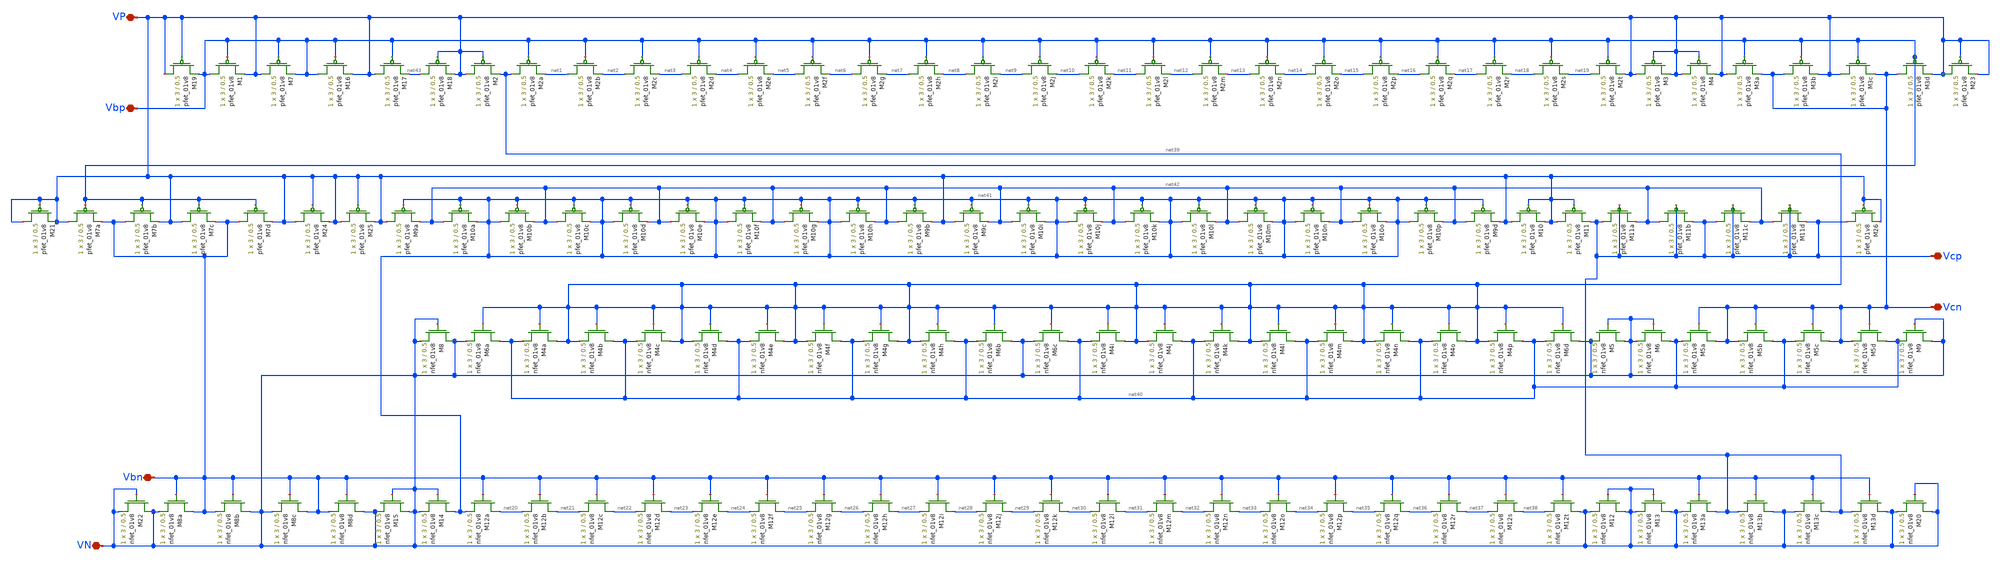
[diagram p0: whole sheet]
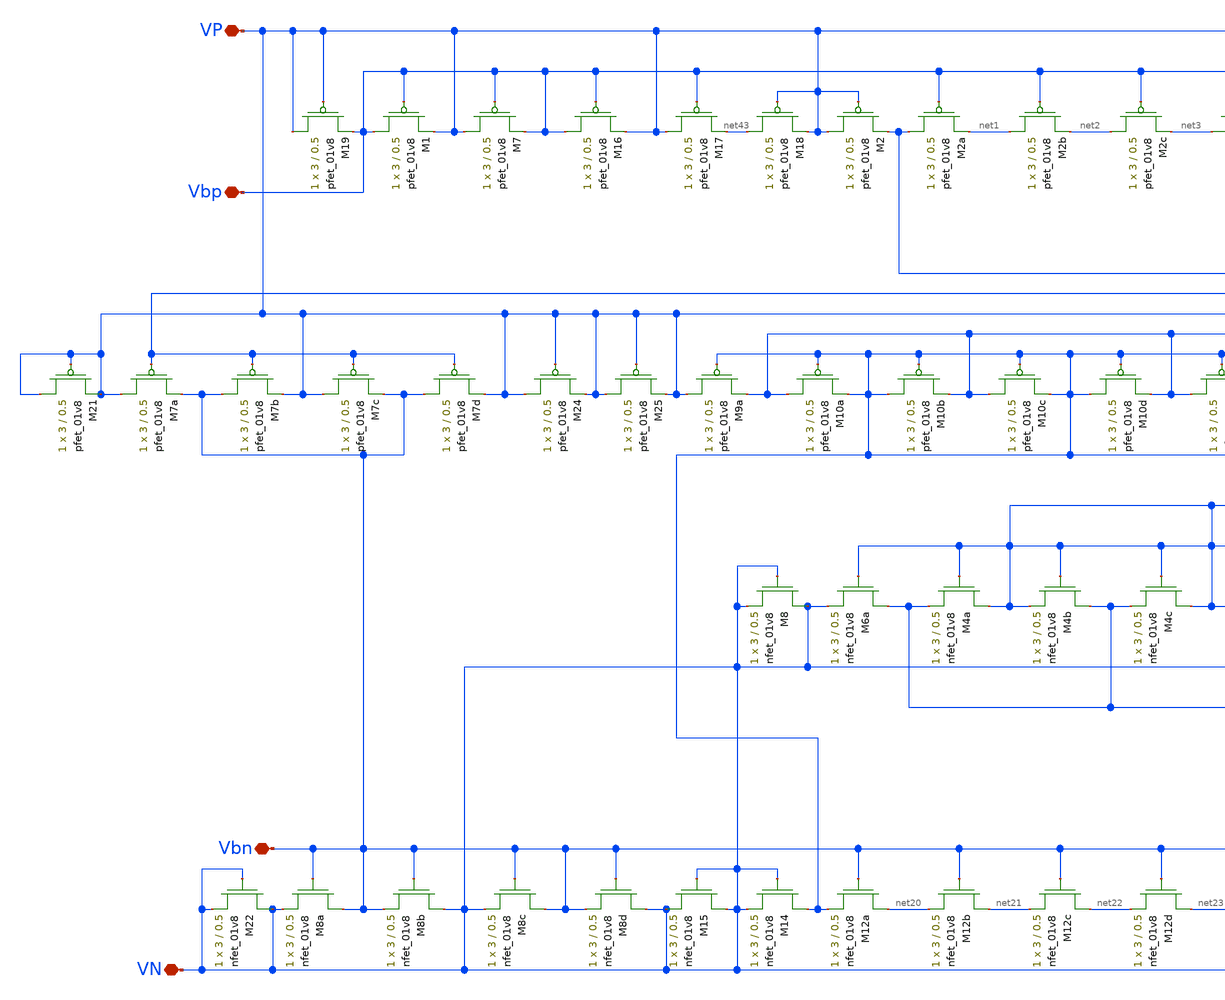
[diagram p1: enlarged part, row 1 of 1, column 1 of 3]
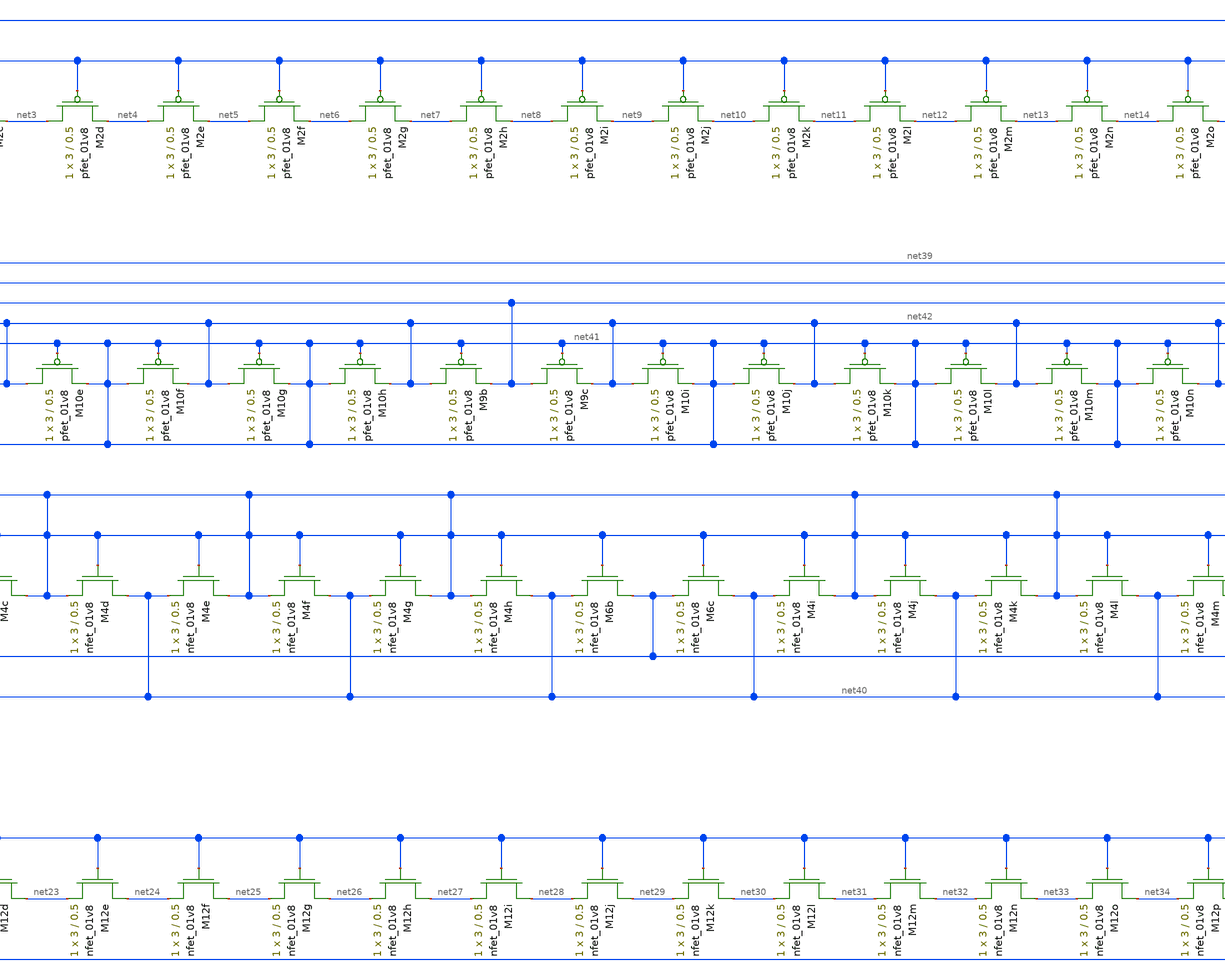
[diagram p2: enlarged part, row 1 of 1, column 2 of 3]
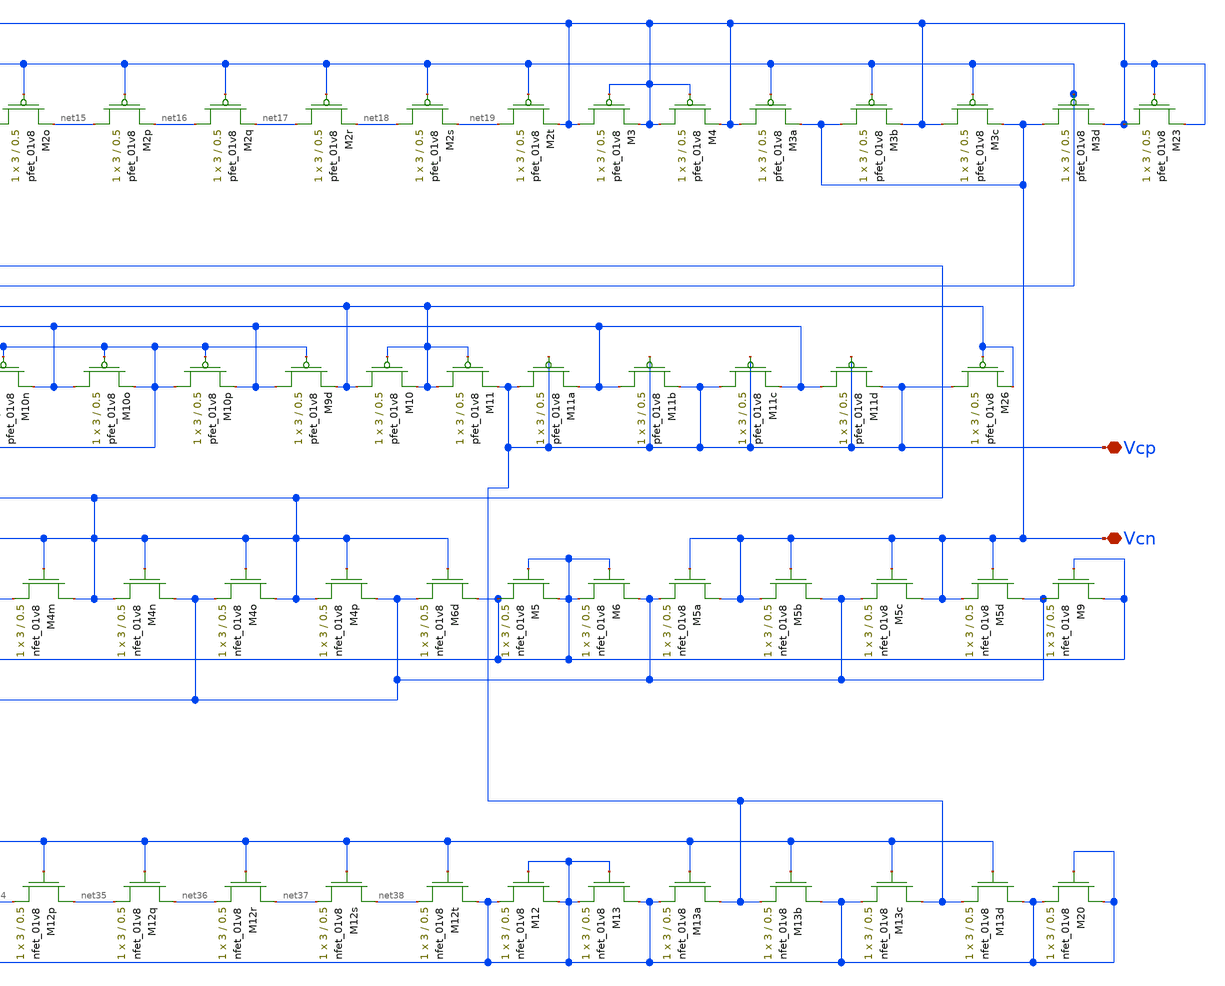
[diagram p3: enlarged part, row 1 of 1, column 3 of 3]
** sch_path: Miniproject3/fcbias.sch
**.subckt fcbias VP VN Vbp Vbn Vcp Vcn
*.iopin VP
*.iopin VN
*.iopin Vbp
*.iopin Vbn
*.iopin Vcp
*.iopin Vcn
XM2a net39 Vbp net1 VDD sky130_fd_pr__pfet_01v8 L=0.5 W=3 nf=1 ad='int((nf+1)/2) * W/nf * 0.29' as='int((nf+2)/2) * W/nf * 0.29'
+ pd='2*int((nf+1)/2) * (W/nf + 0.29)' ps='2*int((nf+2)/2) * (W/nf + 0.29)' nrd='0.29 / W' nrs='0.29 / W'
+ sa=0 sb=0 sd=0 mult=1 m=1
XM12a net20 Vbn net41 GND sky130_fd_pr__nfet_01v8 L=0.5 W=3 nf=1 ad='int((nf+1)/2) * W/nf * 0.29' as='int((nf+2)/2) * W/nf * 0.29'
+ pd='2*int((nf+1)/2) * (W/nf + 0.29)' ps='2*int((nf+2)/2) * (W/nf + 0.29)' nrd='0.29 / W' nrs='0.29 / W'
+ sa=0 sb=0 sd=0 mult=1 m=1
XM12b net21 Vbn net20 GND sky130_fd_pr__nfet_01v8 L=0.5 W=3 nf=1 ad='int((nf+1)/2) * W/nf * 0.29' as='int((nf+2)/2) * W/nf * 0.29'
+ pd='2*int((nf+1)/2) * (W/nf + 0.29)' ps='2*int((nf+2)/2) * (W/nf + 0.29)' nrd='0.29 / W' nrs='0.29 / W'
+ sa=0 sb=0 sd=0 mult=1 m=1
XM12c net22 Vbn net21 GND sky130_fd_pr__nfet_01v8 L=0.5 W=3 nf=1 ad='int((nf+1)/2) * W/nf * 0.29' as='int((nf+2)/2) * W/nf * 0.29'
+ pd='2*int((nf+1)/2) * (W/nf + 0.29)' ps='2*int((nf+2)/2) * (W/nf + 0.29)' nrd='0.29 / W' nrs='0.29 / W'
+ sa=0 sb=0 sd=0 mult=1 m=1
XM12d net23 Vbn net22 GND sky130_fd_pr__nfet_01v8 L=0.5 W=3 nf=1 ad='int((nf+1)/2) * W/nf * 0.29' as='int((nf+2)/2) * W/nf * 0.29'
+ pd='2*int((nf+1)/2) * (W/nf + 0.29)' ps='2*int((nf+2)/2) * (W/nf + 0.29)' nrd='0.29 / W' nrs='0.29 / W'
+ sa=0 sb=0 sd=0 mult=1 m=1
XM12e net24 Vbn net23 GND sky130_fd_pr__nfet_01v8 L=0.5 W=3 nf=1 ad='int((nf+1)/2) * W/nf * 0.29' as='int((nf+2)/2) * W/nf * 0.29'
+ pd='2*int((nf+1)/2) * (W/nf + 0.29)' ps='2*int((nf+2)/2) * (W/nf + 0.29)' nrd='0.29 / W' nrs='0.29 / W'
+ sa=0 sb=0 sd=0 mult=1 m=1
XM12f net25 Vbn net24 GND sky130_fd_pr__nfet_01v8 L=0.5 W=3 nf=1 ad='int((nf+1)/2) * W/nf * 0.29' as='int((nf+2)/2) * W/nf * 0.29'
+ pd='2*int((nf+1)/2) * (W/nf + 0.29)' ps='2*int((nf+2)/2) * (W/nf + 0.29)' nrd='0.29 / W' nrs='0.29 / W'
+ sa=0 sb=0 sd=0 mult=1 m=1
XM12g net26 Vbn net25 GND sky130_fd_pr__nfet_01v8 L=0.5 W=3 nf=1 ad='int((nf+1)/2) * W/nf * 0.29' as='int((nf+2)/2) * W/nf * 0.29'
+ pd='2*int((nf+1)/2) * (W/nf + 0.29)' ps='2*int((nf+2)/2) * (W/nf + 0.29)' nrd='0.29 / W' nrs='0.29 / W'
+ sa=0 sb=0 sd=0 mult=1 m=1
XM12h net27 Vbn net26 GND sky130_fd_pr__nfet_01v8 L=0.5 W=3 nf=1 ad='int((nf+1)/2) * W/nf * 0.29' as='int((nf+2)/2) * W/nf * 0.29'
+ pd='2*int((nf+1)/2) * (W/nf + 0.29)' ps='2*int((nf+2)/2) * (W/nf + 0.29)' nrd='0.29 / W' nrs='0.29 / W'
+ sa=0 sb=0 sd=0 mult=1 m=1
XM12i net28 Vbn net27 GND sky130_fd_pr__nfet_01v8 L=0.5 W=3 nf=1 ad='int((nf+1)/2) * W/nf * 0.29' as='int((nf+2)/2) * W/nf * 0.29'
+ pd='2*int((nf+1)/2) * (W/nf + 0.29)' ps='2*int((nf+2)/2) * (W/nf + 0.29)' nrd='0.29 / W' nrs='0.29 / W'
+ sa=0 sb=0 sd=0 mult=1 m=1
XM12j net29 Vbn net28 GND sky130_fd_pr__nfet_01v8 L=0.5 W=3 nf=1 ad='int((nf+1)/2) * W/nf * 0.29' as='int((nf+2)/2) * W/nf * 0.29'
+ pd='2*int((nf+1)/2) * (W/nf + 0.29)' ps='2*int((nf+2)/2) * (W/nf + 0.29)' nrd='0.29 / W' nrs='0.29 / W'
+ sa=0 sb=0 sd=0 mult=1 m=1
XM12k net30 Vbn net29 GND sky130_fd_pr__nfet_01v8 L=0.5 W=3 nf=1 ad='int((nf+1)/2) * W/nf * 0.29' as='int((nf+2)/2) * W/nf * 0.29'
+ pd='2*int((nf+1)/2) * (W/nf + 0.29)' ps='2*int((nf+2)/2) * (W/nf + 0.29)' nrd='0.29 / W' nrs='0.29 / W'
+ sa=0 sb=0 sd=0 mult=1 m=1
XM12l net31 Vbn net30 GND sky130_fd_pr__nfet_01v8 L=0.5 W=3 nf=1 ad='int((nf+1)/2) * W/nf * 0.29' as='int((nf+2)/2) * W/nf * 0.29'
+ pd='2*int((nf+1)/2) * (W/nf + 0.29)' ps='2*int((nf+2)/2) * (W/nf + 0.29)' nrd='0.29 / W' nrs='0.29 / W'
+ sa=0 sb=0 sd=0 mult=1 m=1
XM12m net32 Vbn net31 GND sky130_fd_pr__nfet_01v8 L=0.5 W=3 nf=1 ad='int((nf+1)/2) * W/nf * 0.29' as='int((nf+2)/2) * W/nf * 0.29'
+ pd='2*int((nf+1)/2) * (W/nf + 0.29)' ps='2*int((nf+2)/2) * (W/nf + 0.29)' nrd='0.29 / W' nrs='0.29 / W'
+ sa=0 sb=0 sd=0 mult=1 m=1
XM12n net33 Vbn net32 GND sky130_fd_pr__nfet_01v8 L=0.5 W=3 nf=1 ad='int((nf+1)/2) * W/nf * 0.29' as='int((nf+2)/2) * W/nf * 0.29'
+ pd='2*int((nf+1)/2) * (W/nf + 0.29)' ps='2*int((nf+2)/2) * (W/nf + 0.29)' nrd='0.29 / W' nrs='0.29 / W'
+ sa=0 sb=0 sd=0 mult=1 m=1
XM12o net34 Vbn net33 GND sky130_fd_pr__nfet_01v8 L=0.5 W=3 nf=1 ad='int((nf+1)/2) * W/nf * 0.29' as='int((nf+2)/2) * W/nf * 0.29'
+ pd='2*int((nf+1)/2) * (W/nf + 0.29)' ps='2*int((nf+2)/2) * (W/nf + 0.29)' nrd='0.29 / W' nrs='0.29 / W'
+ sa=0 sb=0 sd=0 mult=1 m=1
XM12p net35 Vbn net34 GND sky130_fd_pr__nfet_01v8 L=0.5 W=3 nf=1 ad='int((nf+1)/2) * W/nf * 0.29' as='int((nf+2)/2) * W/nf * 0.29'
+ pd='2*int((nf+1)/2) * (W/nf + 0.29)' ps='2*int((nf+2)/2) * (W/nf + 0.29)' nrd='0.29 / W' nrs='0.29 / W'
+ sa=0 sb=0 sd=0 mult=1 m=1
XM12q net36 Vbn net35 GND sky130_fd_pr__nfet_01v8 L=0.5 W=3 nf=1 ad='int((nf+1)/2) * W/nf * 0.29' as='int((nf+2)/2) * W/nf * 0.29'
+ pd='2*int((nf+1)/2) * (W/nf + 0.29)' ps='2*int((nf+2)/2) * (W/nf + 0.29)' nrd='0.29 / W' nrs='0.29 / W'
+ sa=0 sb=0 sd=0 mult=1 m=1
XM12r net37 Vbn net36 GND sky130_fd_pr__nfet_01v8 L=0.5 W=3 nf=1 ad='int((nf+1)/2) * W/nf * 0.29' as='int((nf+2)/2) * W/nf * 0.29'
+ pd='2*int((nf+1)/2) * (W/nf + 0.29)' ps='2*int((nf+2)/2) * (W/nf + 0.29)' nrd='0.29 / W' nrs='0.29 / W'
+ sa=0 sb=0 sd=0 mult=1 m=1
XM12s net38 Vbn net37 GND sky130_fd_pr__nfet_01v8 L=0.5 W=3 nf=1 ad='int((nf+1)/2) * W/nf * 0.29' as='int((nf+2)/2) * W/nf * 0.29'
+ pd='2*int((nf+1)/2) * (W/nf + 0.29)' ps='2*int((nf+2)/2) * (W/nf + 0.29)' nrd='0.29 / W' nrs='0.29 / W'
+ sa=0 sb=0 sd=0 mult=1 m=1
XM12t VN Vbn net38 GND sky130_fd_pr__nfet_01v8 L=0.5 W=3 nf=1 ad='int((nf+1)/2) * W/nf * 0.29' as='int((nf+2)/2) * W/nf * 0.29'
+ pd='2*int((nf+1)/2) * (W/nf + 0.29)' ps='2*int((nf+2)/2) * (W/nf + 0.29)' nrd='0.29 / W' nrs='0.29 / W'
+ sa=0 sb=0 sd=0 mult=1 m=1
XM2b net1 Vbp net2 VDD sky130_fd_pr__pfet_01v8 L=0.5 W=3 nf=1 ad='int((nf+1)/2) * W/nf * 0.29' as='int((nf+2)/2) * W/nf * 0.29'
+ pd='2*int((nf+1)/2) * (W/nf + 0.29)' ps='2*int((nf+2)/2) * (W/nf + 0.29)' nrd='0.29 / W' nrs='0.29 / W'
+ sa=0 sb=0 sd=0 mult=1 m=1
XM2c net2 Vbp net3 VDD sky130_fd_pr__pfet_01v8 L=0.5 W=3 nf=1 ad='int((nf+1)/2) * W/nf * 0.29' as='int((nf+2)/2) * W/nf * 0.29'
+ pd='2*int((nf+1)/2) * (W/nf + 0.29)' ps='2*int((nf+2)/2) * (W/nf + 0.29)' nrd='0.29 / W' nrs='0.29 / W'
+ sa=0 sb=0 sd=0 mult=1 m=1
XM2d net3 Vbp net4 VDD sky130_fd_pr__pfet_01v8 L=0.5 W=3 nf=1 ad='int((nf+1)/2) * W/nf * 0.29' as='int((nf+2)/2) * W/nf * 0.29'
+ pd='2*int((nf+1)/2) * (W/nf + 0.29)' ps='2*int((nf+2)/2) * (W/nf + 0.29)' nrd='0.29 / W' nrs='0.29 / W'
+ sa=0 sb=0 sd=0 mult=1 m=1
XM2e net4 Vbp net5 VDD sky130_fd_pr__pfet_01v8 L=0.5 W=3 nf=1 ad='int((nf+1)/2) * W/nf * 0.29' as='int((nf+2)/2) * W/nf * 0.29'
+ pd='2*int((nf+1)/2) * (W/nf + 0.29)' ps='2*int((nf+2)/2) * (W/nf + 0.29)' nrd='0.29 / W' nrs='0.29 / W'
+ sa=0 sb=0 sd=0 mult=1 m=1
XM2f net5 Vbp net6 VDD sky130_fd_pr__pfet_01v8 L=0.5 W=3 nf=1 ad='int((nf+1)/2) * W/nf * 0.29' as='int((nf+2)/2) * W/nf * 0.29'
+ pd='2*int((nf+1)/2) * (W/nf + 0.29)' ps='2*int((nf+2)/2) * (W/nf + 0.29)' nrd='0.29 / W' nrs='0.29 / W'
+ sa=0 sb=0 sd=0 mult=1 m=1
XM2g net6 Vbp net7 VDD sky130_fd_pr__pfet_01v8 L=0.5 W=3 nf=1 ad='int((nf+1)/2) * W/nf * 0.29' as='int((nf+2)/2) * W/nf * 0.29'
+ pd='2*int((nf+1)/2) * (W/nf + 0.29)' ps='2*int((nf+2)/2) * (W/nf + 0.29)' nrd='0.29 / W' nrs='0.29 / W'
+ sa=0 sb=0 sd=0 mult=1 m=1
XM2h net7 Vbp net8 VDD sky130_fd_pr__pfet_01v8 L=0.5 W=3 nf=1 ad='int((nf+1)/2) * W/nf * 0.29' as='int((nf+2)/2) * W/nf * 0.29'
+ pd='2*int((nf+1)/2) * (W/nf + 0.29)' ps='2*int((nf+2)/2) * (W/nf + 0.29)' nrd='0.29 / W' nrs='0.29 / W'
+ sa=0 sb=0 sd=0 mult=1 m=1
XM2i net8 Vbp net9 VDD sky130_fd_pr__pfet_01v8 L=0.5 W=3 nf=1 ad='int((nf+1)/2) * W/nf * 0.29' as='int((nf+2)/2) * W/nf * 0.29'
+ pd='2*int((nf+1)/2) * (W/nf + 0.29)' ps='2*int((nf+2)/2) * (W/nf + 0.29)' nrd='0.29 / W' nrs='0.29 / W'
+ sa=0 sb=0 sd=0 mult=1 m=1
XM2j net9 Vbp net10 VDD sky130_fd_pr__pfet_01v8 L=0.5 W=3 nf=1 ad='int((nf+1)/2) * W/nf * 0.29' as='int((nf+2)/2) * W/nf * 0.29'
+ pd='2*int((nf+1)/2) * (W/nf + 0.29)' ps='2*int((nf+2)/2) * (W/nf + 0.29)' nrd='0.29 / W' nrs='0.29 / W'
+ sa=0 sb=0 sd=0 mult=1 m=1
XM2k net10 Vbp net11 VDD sky130_fd_pr__pfet_01v8 L=0.5 W=3 nf=1 ad='int((nf+1)/2) * W/nf * 0.29' as='int((nf+2)/2) * W/nf * 0.29'
+ pd='2*int((nf+1)/2) * (W/nf + 0.29)' ps='2*int((nf+2)/2) * (W/nf + 0.29)' nrd='0.29 / W' nrs='0.29 / W'
+ sa=0 sb=0 sd=0 mult=1 m=1
XM2l net11 Vbp net12 VDD sky130_fd_pr__pfet_01v8 L=0.5 W=3 nf=1 ad='int((nf+1)/2) * W/nf * 0.29' as='int((nf+2)/2) * W/nf * 0.29'
+ pd='2*int((nf+1)/2) * (W/nf + 0.29)' ps='2*int((nf+2)/2) * (W/nf + 0.29)' nrd='0.29 / W' nrs='0.29 / W'
+ sa=0 sb=0 sd=0 mult=1 m=1
XM2m net12 Vbp net13 VDD sky130_fd_pr__pfet_01v8 L=0.5 W=3 nf=1 ad='int((nf+1)/2) * W/nf * 0.29' as='int((nf+2)/2) * W/nf * 0.29'
+ pd='2*int((nf+1)/2) * (W/nf + 0.29)' ps='2*int((nf+2)/2) * (W/nf + 0.29)' nrd='0.29 / W' nrs='0.29 / W'
+ sa=0 sb=0 sd=0 mult=1 m=1
XM2n net13 Vbp net14 VDD sky130_fd_pr__pfet_01v8 L=0.5 W=3 nf=1 ad='int((nf+1)/2) * W/nf * 0.29' as='int((nf+2)/2) * W/nf * 0.29'
+ pd='2*int((nf+1)/2) * (W/nf + 0.29)' ps='2*int((nf+2)/2) * (W/nf + 0.29)' nrd='0.29 / W' nrs='0.29 / W'
+ sa=0 sb=0 sd=0 mult=1 m=1
XM2o net14 Vbp net15 VDD sky130_fd_pr__pfet_01v8 L=0.5 W=3 nf=1 ad='int((nf+1)/2) * W/nf * 0.29' as='int((nf+2)/2) * W/nf * 0.29'
+ pd='2*int((nf+1)/2) * (W/nf + 0.29)' ps='2*int((nf+2)/2) * (W/nf + 0.29)' nrd='0.29 / W' nrs='0.29 / W'
+ sa=0 sb=0 sd=0 mult=1 m=1
XM2p net15 Vbp net16 VDD sky130_fd_pr__pfet_01v8 L=0.5 W=3 nf=1 ad='int((nf+1)/2) * W/nf * 0.29' as='int((nf+2)/2) * W/nf * 0.29'
+ pd='2*int((nf+1)/2) * (W/nf + 0.29)' ps='2*int((nf+2)/2) * (W/nf + 0.29)' nrd='0.29 / W' nrs='0.29 / W'
+ sa=0 sb=0 sd=0 mult=1 m=1
XM2q net16 Vbp net17 VDD sky130_fd_pr__pfet_01v8 L=0.5 W=3 nf=1 ad='int((nf+1)/2) * W/nf * 0.29' as='int((nf+2)/2) * W/nf * 0.29'
+ pd='2*int((nf+1)/2) * (W/nf + 0.29)' ps='2*int((nf+2)/2) * (W/nf + 0.29)' nrd='0.29 / W' nrs='0.29 / W'
+ sa=0 sb=0 sd=0 mult=1 m=1
XM2r net17 Vbp net18 VDD sky130_fd_pr__pfet_01v8 L=0.5 W=3 nf=1 ad='int((nf+1)/2) * W/nf * 0.29' as='int((nf+2)/2) * W/nf * 0.29'
+ pd='2*int((nf+1)/2) * (W/nf + 0.29)' ps='2*int((nf+2)/2) * (W/nf + 0.29)' nrd='0.29 / W' nrs='0.29 / W'
+ sa=0 sb=0 sd=0 mult=1 m=1
XM2s net18 Vbp net19 VDD sky130_fd_pr__pfet_01v8 L=0.5 W=3 nf=1 ad='int((nf+1)/2) * W/nf * 0.29' as='int((nf+2)/2) * W/nf * 0.29'
+ pd='2*int((nf+1)/2) * (W/nf + 0.29)' ps='2*int((nf+2)/2) * (W/nf + 0.29)' nrd='0.29 / W' nrs='0.29 / W'
+ sa=0 sb=0 sd=0 mult=1 m=1
XM2t net19 Vbp VP VDD sky130_fd_pr__pfet_01v8 L=0.5 W=3 nf=1 ad='int((nf+1)/2) * W/nf * 0.29' as='int((nf+2)/2) * W/nf * 0.29'
+ pd='2*int((nf+1)/2) * (W/nf + 0.29)' ps='2*int((nf+2)/2) * (W/nf + 0.29)' nrd='0.29 / W' nrs='0.29 / W'
+ sa=0 sb=0 sd=0 mult=1 m=1
XM4a net39 net39 net40 GND sky130_fd_pr__nfet_01v8 L=0.5 W=3 nf=1 ad='int((nf+1)/2) * W/nf * 0.29' as='int((nf+2)/2) * W/nf * 0.29'
+ pd='2*int((nf+1)/2) * (W/nf + 0.29)' ps='2*int((nf+2)/2) * (W/nf + 0.29)' nrd='0.29 / W' nrs='0.29 / W'
+ sa=0 sb=0 sd=0 mult=1 m=1
XM4b net40 net39 net39 GND sky130_fd_pr__nfet_01v8 L=0.5 W=3 nf=1 ad='int((nf+1)/2) * W/nf * 0.29' as='int((nf+2)/2) * W/nf * 0.29'
+ pd='2*int((nf+1)/2) * (W/nf + 0.29)' ps='2*int((nf+2)/2) * (W/nf + 0.29)' nrd='0.29 / W' nrs='0.29 / W'
+ sa=0 sb=0 sd=0 mult=1 m=1
XM4c net39 net39 net40 GND sky130_fd_pr__nfet_01v8 L=0.5 W=3 nf=1 ad='int((nf+1)/2) * W/nf * 0.29' as='int((nf+2)/2) * W/nf * 0.29'
+ pd='2*int((nf+1)/2) * (W/nf + 0.29)' ps='2*int((nf+2)/2) * (W/nf + 0.29)' nrd='0.29 / W' nrs='0.29 / W'
+ sa=0 sb=0 sd=0 mult=1 m=1
XM4d net40 net39 net39 GND sky130_fd_pr__nfet_01v8 L=0.5 W=3 nf=1 ad='int((nf+1)/2) * W/nf * 0.29' as='int((nf+2)/2) * W/nf * 0.29'
+ pd='2*int((nf+1)/2) * (W/nf + 0.29)' ps='2*int((nf+2)/2) * (W/nf + 0.29)' nrd='0.29 / W' nrs='0.29 / W'
+ sa=0 sb=0 sd=0 mult=1 m=1
XM4e net39 net39 net40 GND sky130_fd_pr__nfet_01v8 L=0.5 W=3 nf=1 ad='int((nf+1)/2) * W/nf * 0.29' as='int((nf+2)/2) * W/nf * 0.29'
+ pd='2*int((nf+1)/2) * (W/nf + 0.29)' ps='2*int((nf+2)/2) * (W/nf + 0.29)' nrd='0.29 / W' nrs='0.29 / W'
+ sa=0 sb=0 sd=0 mult=1 m=1
XM4f net40 net39 net39 GND sky130_fd_pr__nfet_01v8 L=0.5 W=3 nf=1 ad='int((nf+1)/2) * W/nf * 0.29' as='int((nf+2)/2) * W/nf * 0.29'
+ pd='2*int((nf+1)/2) * (W/nf + 0.29)' ps='2*int((nf+2)/2) * (W/nf + 0.29)' nrd='0.29 / W' nrs='0.29 / W'
+ sa=0 sb=0 sd=0 mult=1 m=1
XM4g net39 net39 net40 GND sky130_fd_pr__nfet_01v8 L=0.5 W=3 nf=1 ad='int((nf+1)/2) * W/nf * 0.29' as='int((nf+2)/2) * W/nf * 0.29'
+ pd='2*int((nf+1)/2) * (W/nf + 0.29)' ps='2*int((nf+2)/2) * (W/nf + 0.29)' nrd='0.29 / W' nrs='0.29 / W'
+ sa=0 sb=0 sd=0 mult=1 m=1
XM4h net40 net39 net39 GND sky130_fd_pr__nfet_01v8 L=0.5 W=3 nf=1 ad='int((nf+1)/2) * W/nf * 0.29' as='int((nf+2)/2) * W/nf * 0.29'
+ pd='2*int((nf+1)/2) * (W/nf + 0.29)' ps='2*int((nf+2)/2) * (W/nf + 0.29)' nrd='0.29 / W' nrs='0.29 / W'
+ sa=0 sb=0 sd=0 mult=1 m=1
XM4i net39 net39 net40 GND sky130_fd_pr__nfet_01v8 L=0.5 W=3 nf=1 ad='int((nf+1)/2) * W/nf * 0.29' as='int((nf+2)/2) * W/nf * 0.29'
+ pd='2*int((nf+1)/2) * (W/nf + 0.29)' ps='2*int((nf+2)/2) * (W/nf + 0.29)' nrd='0.29 / W' nrs='0.29 / W'
+ sa=0 sb=0 sd=0 mult=1 m=1
XM4j net40 net39 net39 GND sky130_fd_pr__nfet_01v8 L=0.5 W=3 nf=1 ad='int((nf+1)/2) * W/nf * 0.29' as='int((nf+2)/2) * W/nf * 0.29'
+ pd='2*int((nf+1)/2) * (W/nf + 0.29)' ps='2*int((nf+2)/2) * (W/nf + 0.29)' nrd='0.29 / W' nrs='0.29 / W'
+ sa=0 sb=0 sd=0 mult=1 m=1
XM4k net39 net39 net40 GND sky130_fd_pr__nfet_01v8 L=0.5 W=3 nf=1 ad='int((nf+1)/2) * W/nf * 0.29' as='int((nf+2)/2) * W/nf * 0.29'
+ pd='2*int((nf+1)/2) * (W/nf + 0.29)' ps='2*int((nf+2)/2) * (W/nf + 0.29)' nrd='0.29 / W' nrs='0.29 / W'
+ sa=0 sb=0 sd=0 mult=1 m=1
XM4l net40 net39 net39 GND sky130_fd_pr__nfet_01v8 L=0.5 W=3 nf=1 ad='int((nf+1)/2) * W/nf * 0.29' as='int((nf+2)/2) * W/nf * 0.29'
+ pd='2*int((nf+1)/2) * (W/nf + 0.29)' ps='2*int((nf+2)/2) * (W/nf + 0.29)' nrd='0.29 / W' nrs='0.29 / W'
+ sa=0 sb=0 sd=0 mult=1 m=1
XM4m net39 net39 net40 GND sky130_fd_pr__nfet_01v8 L=0.5 W=3 nf=1 ad='int((nf+1)/2) * W/nf * 0.29' as='int((nf+2)/2) * W/nf * 0.29'
+ pd='2*int((nf+1)/2) * (W/nf + 0.29)' ps='2*int((nf+2)/2) * (W/nf + 0.29)' nrd='0.29 / W' nrs='0.29 / W'
+ sa=0 sb=0 sd=0 mult=1 m=1
XM4n net40 net39 net39 GND sky130_fd_pr__nfet_01v8 L=0.5 W=3 nf=1 ad='int((nf+1)/2) * W/nf * 0.29' as='int((nf+2)/2) * W/nf * 0.29'
+ pd='2*int((nf+1)/2) * (W/nf + 0.29)' ps='2*int((nf+2)/2) * (W/nf + 0.29)' nrd='0.29 / W' nrs='0.29 / W'
+ sa=0 sb=0 sd=0 mult=1 m=1
XM4o net39 net39 net40 GND sky130_fd_pr__nfet_01v8 L=0.5 W=3 nf=1 ad='int((nf+1)/2) * W/nf * 0.29' as='int((nf+2)/2) * W/nf * 0.29'
+ pd='2*int((nf+1)/2) * (W/nf + 0.29)' ps='2*int((nf+2)/2) * (W/nf + 0.29)' nrd='0.29 / W' nrs='0.29 / W'
+ sa=0 sb=0 sd=0 mult=1 m=1
XM4p net40 net39 net39 GND sky130_fd_pr__nfet_01v8 L=0.5 W=3 nf=1 ad='int((nf+1)/2) * W/nf * 0.29' as='int((nf+2)/2) * W/nf * 0.29'
+ pd='2*int((nf+1)/2) * (W/nf + 0.29)' ps='2*int((nf+2)/2) * (W/nf + 0.29)' nrd='0.29 / W' nrs='0.29 / W'
+ sa=0 sb=0 sd=0 mult=1 m=1
XM10a net42 net41 net41 VDD sky130_fd_pr__pfet_01v8 L=0.5 W=3 nf=1 ad='int((nf+1)/2) * W/nf * 0.29' as='int((nf+2)/2) * W/nf * 0.29'
+ pd='2*int((nf+1)/2) * (W/nf + 0.29)' ps='2*int((nf+2)/2) * (W/nf + 0.29)' nrd='0.29 / W' nrs='0.29 / W'
+ sa=0 sb=0 sd=0 mult=1 m=1
XM10b net41 net41 net42 VDD sky130_fd_pr__pfet_01v8 L=0.5 W=3 nf=1 ad='int((nf+1)/2) * W/nf * 0.29' as='int((nf+2)/2) * W/nf * 0.29'
+ pd='2*int((nf+1)/2) * (W/nf + 0.29)' ps='2*int((nf+2)/2) * (W/nf + 0.29)' nrd='0.29 / W' nrs='0.29 / W'
+ sa=0 sb=0 sd=0 mult=1 m=1
XM10c net42 net41 net41 VDD sky130_fd_pr__pfet_01v8 L=0.5 W=3 nf=1 ad='int((nf+1)/2) * W/nf * 0.29' as='int((nf+2)/2) * W/nf * 0.29'
+ pd='2*int((nf+1)/2) * (W/nf + 0.29)' ps='2*int((nf+2)/2) * (W/nf + 0.29)' nrd='0.29 / W' nrs='0.29 / W'
+ sa=0 sb=0 sd=0 mult=1 m=1
XM10d net41 net41 net42 VDD sky130_fd_pr__pfet_01v8 L=0.5 W=3 nf=1 ad='int((nf+1)/2) * W/nf * 0.29' as='int((nf+2)/2) * W/nf * 0.29'
+ pd='2*int((nf+1)/2) * (W/nf + 0.29)' ps='2*int((nf+2)/2) * (W/nf + 0.29)' nrd='0.29 / W' nrs='0.29 / W'
+ sa=0 sb=0 sd=0 mult=1 m=1
XM10e net42 net41 net41 VDD sky130_fd_pr__pfet_01v8 L=0.5 W=3 nf=1 ad='int((nf+1)/2) * W/nf * 0.29' as='int((nf+2)/2) * W/nf * 0.29'
+ pd='2*int((nf+1)/2) * (W/nf + 0.29)' ps='2*int((nf+2)/2) * (W/nf + 0.29)' nrd='0.29 / W' nrs='0.29 / W'
+ sa=0 sb=0 sd=0 mult=1 m=1
XM10f net41 net41 net42 VDD sky130_fd_pr__pfet_01v8 L=0.5 W=3 nf=1 ad='int((nf+1)/2) * W/nf * 0.29' as='int((nf+2)/2) * W/nf * 0.29'
+ pd='2*int((nf+1)/2) * (W/nf + 0.29)' ps='2*int((nf+2)/2) * (W/nf + 0.29)' nrd='0.29 / W' nrs='0.29 / W'
+ sa=0 sb=0 sd=0 mult=1 m=1
XM10g net42 net41 net41 VDD sky130_fd_pr__pfet_01v8 L=0.5 W=3 nf=1 ad='int((nf+1)/2) * W/nf * 0.29' as='int((nf+2)/2) * W/nf * 0.29'
+ pd='2*int((nf+1)/2) * (W/nf + 0.29)' ps='2*int((nf+2)/2) * (W/nf + 0.29)' nrd='0.29 / W' nrs='0.29 / W'
+ sa=0 sb=0 sd=0 mult=1 m=1
XM10h net41 net41 net42 VDD sky130_fd_pr__pfet_01v8 L=0.5 W=3 nf=1 ad='int((nf+1)/2) * W/nf * 0.29' as='int((nf+2)/2) * W/nf * 0.29'
+ pd='2*int((nf+1)/2) * (W/nf + 0.29)' ps='2*int((nf+2)/2) * (W/nf + 0.29)' nrd='0.29 / W' nrs='0.29 / W'
+ sa=0 sb=0 sd=0 mult=1 m=1
XM10i net42 net41 net41 VDD sky130_fd_pr__pfet_01v8 L=0.5 W=3 nf=1 ad='int((nf+1)/2) * W/nf * 0.29' as='int((nf+2)/2) * W/nf * 0.29'
+ pd='2*int((nf+1)/2) * (W/nf + 0.29)' ps='2*int((nf+2)/2) * (W/nf + 0.29)' nrd='0.29 / W' nrs='0.29 / W'
+ sa=0 sb=0 sd=0 mult=1 m=1
XM10j net41 net41 net42 VDD sky130_fd_pr__pfet_01v8 L=0.5 W=3 nf=1 ad='int((nf+1)/2) * W/nf * 0.29' as='int((nf+2)/2) * W/nf * 0.29'
+ pd='2*int((nf+1)/2) * (W/nf + 0.29)' ps='2*int((nf+2)/2) * (W/nf + 0.29)' nrd='0.29 / W' nrs='0.29 / W'
+ sa=0 sb=0 sd=0 mult=1 m=1
XM10k net42 net41 net41 VDD sky130_fd_pr__pfet_01v8 L=0.5 W=3 nf=1 ad='int((nf+1)/2) * W/nf * 0.29' as='int((nf+2)/2) * W/nf * 0.29'
+ pd='2*int((nf+1)/2) * (W/nf + 0.29)' ps='2*int((nf+2)/2) * (W/nf + 0.29)' nrd='0.29 / W' nrs='0.29 / W'
+ sa=0 sb=0 sd=0 mult=1 m=1
XM10l net41 net41 net42 VDD sky130_fd_pr__pfet_01v8 L=0.5 W=3 nf=1 ad='int((nf+1)/2) * W/nf * 0.29' as='int((nf+2)/2) * W/nf * 0.29'
+ pd='2*int((nf+1)/2) * (W/nf + 0.29)' ps='2*int((nf+2)/2) * (W/nf + 0.29)' nrd='0.29 / W' nrs='0.29 / W'
+ sa=0 sb=0 sd=0 mult=1 m=1
XM10m net42 net41 net41 VDD sky130_fd_pr__pfet_01v8 L=0.5 W=3 nf=1 ad='int((nf+1)/2) * W/nf * 0.29' as='int((nf+2)/2) * W/nf * 0.29'
+ pd='2*int((nf+1)/2) * (W/nf + 0.29)' ps='2*int((nf+2)/2) * (W/nf + 0.29)' nrd='0.29 / W' nrs='0.29 / W'
+ sa=0 sb=0 sd=0 mult=1 m=1
XM10n net41 net41 net42 VDD sky130_fd_pr__pfet_01v8 L=0.5 W=3 nf=1 ad='int((nf+1)/2) * W/nf * 0.29' as='int((nf+2)/2) * W/nf * 0.29'
+ pd='2*int((nf+1)/2) * (W/nf + 0.29)' ps='2*int((nf+2)/2) * (W/nf + 0.29)' nrd='0.29 / W' nrs='0.29 / W'
+ sa=0 sb=0 sd=0 mult=1 m=1
XM10o net42 net41 net41 VDD sky130_fd_pr__pfet_01v8 L=0.5 W=3 nf=1 ad='int((nf+1)/2) * W/nf * 0.29' as='int((nf+2)/2) * W/nf * 0.29'
+ pd='2*int((nf+1)/2) * (W/nf + 0.29)' ps='2*int((nf+2)/2) * (W/nf + 0.29)' nrd='0.29 / W' nrs='0.29 / W'
+ sa=0 sb=0 sd=0 mult=1 m=1
XM10p net41 net41 net42 VDD sky130_fd_pr__pfet_01v8 L=0.5 W=3 nf=1 ad='int((nf+1)/2) * W/nf * 0.29' as='int((nf+2)/2) * W/nf * 0.29'
+ pd='2*int((nf+1)/2) * (W/nf + 0.29)' ps='2*int((nf+2)/2) * (W/nf + 0.29)' nrd='0.29 / W' nrs='0.29 / W'
+ sa=0 sb=0 sd=0 mult=1 m=1
XM3a VP Vbp Vcn VDD sky130_fd_pr__pfet_01v8 L=0.5 W=3 nf=1 ad='int((nf+1)/2) * W/nf * 0.29' as='int((nf+2)/2) * W/nf * 0.29'
+ pd='2*int((nf+1)/2) * (W/nf + 0.29)' ps='2*int((nf+2)/2) * (W/nf + 0.29)' nrd='0.29 / W' nrs='0.29 / W'
+ sa=0 sb=0 sd=0 mult=1 m=1
XM3b Vcn Vbp VP VDD sky130_fd_pr__pfet_01v8 L=0.5 W=3 nf=1 ad='int((nf+1)/2) * W/nf * 0.29' as='int((nf+2)/2) * W/nf * 0.29'
+ pd='2*int((nf+1)/2) * (W/nf + 0.29)' ps='2*int((nf+2)/2) * (W/nf + 0.29)' nrd='0.29 / W' nrs='0.29 / W'
+ sa=0 sb=0 sd=0 mult=1 m=1
XM3c VP Vbp Vcn VDD sky130_fd_pr__pfet_01v8 L=0.5 W=3 nf=1 ad='int((nf+1)/2) * W/nf * 0.29' as='int((nf+2)/2) * W/nf * 0.29'
+ pd='2*int((nf+1)/2) * (W/nf + 0.29)' ps='2*int((nf+2)/2) * (W/nf + 0.29)' nrd='0.29 / W' nrs='0.29 / W'
+ sa=0 sb=0 sd=0 mult=1 m=1
XM3d Vcn Vbp VP VDD sky130_fd_pr__pfet_01v8 L=0.5 W=3 nf=1 ad='int((nf+1)/2) * W/nf * 0.29' as='int((nf+2)/2) * W/nf * 0.29'
+ pd='2*int((nf+1)/2) * (W/nf + 0.29)' ps='2*int((nf+2)/2) * (W/nf + 0.29)' nrd='0.29 / W' nrs='0.29 / W'
+ sa=0 sb=0 sd=0 mult=1 m=1
XM7a VP Vbp Vbn VDD sky130_fd_pr__pfet_01v8 L=0.5 W=3 nf=1 ad='int((nf+1)/2) * W/nf * 0.29' as='int((nf+2)/2) * W/nf * 0.29'
+ pd='2*int((nf+1)/2) * (W/nf + 0.29)' ps='2*int((nf+2)/2) * (W/nf + 0.29)' nrd='0.29 / W' nrs='0.29 / W'
+ sa=0 sb=0 sd=0 mult=1 m=1
XM7b Vbn Vbp VP VDD sky130_fd_pr__pfet_01v8 L=0.5 W=3 nf=1 ad='int((nf+1)/2) * W/nf * 0.29' as='int((nf+2)/2) * W/nf * 0.29'
+ pd='2*int((nf+1)/2) * (W/nf + 0.29)' ps='2*int((nf+2)/2) * (W/nf + 0.29)' nrd='0.29 / W' nrs='0.29 / W'
+ sa=0 sb=0 sd=0 mult=1 m=1
XM7c VP Vbp Vbn VDD sky130_fd_pr__pfet_01v8 L=0.5 W=3 nf=1 ad='int((nf+1)/2) * W/nf * 0.29' as='int((nf+2)/2) * W/nf * 0.29'
+ pd='2*int((nf+1)/2) * (W/nf + 0.29)' ps='2*int((nf+2)/2) * (W/nf + 0.29)' nrd='0.29 / W' nrs='0.29 / W'
+ sa=0 sb=0 sd=0 mult=1 m=1
XM7d Vbn Vbp VP VDD sky130_fd_pr__pfet_01v8 L=0.5 W=3 nf=1 ad='int((nf+1)/2) * W/nf * 0.29' as='int((nf+2)/2) * W/nf * 0.29'
+ pd='2*int((nf+1)/2) * (W/nf + 0.29)' ps='2*int((nf+2)/2) * (W/nf + 0.29)' nrd='0.29 / W' nrs='0.29 / W'
+ sa=0 sb=0 sd=0 mult=1 m=1
XM9a VP net41 net42 VDD sky130_fd_pr__pfet_01v8 L=0.5 W=3 nf=1 ad='int((nf+1)/2) * W/nf * 0.29' as='int((nf+2)/2) * W/nf * 0.29'
+ pd='2*int((nf+1)/2) * (W/nf + 0.29)' ps='2*int((nf+2)/2) * (W/nf + 0.29)' nrd='0.29 / W' nrs='0.29 / W'
+ sa=0 sb=0 sd=0 mult=1 m=1
XM9b net42 net41 VP VDD sky130_fd_pr__pfet_01v8 L=0.5 W=3 nf=1 ad='int((nf+1)/2) * W/nf * 0.29' as='int((nf+2)/2) * W/nf * 0.29'
+ pd='2*int((nf+1)/2) * (W/nf + 0.29)' ps='2*int((nf+2)/2) * (W/nf + 0.29)' nrd='0.29 / W' nrs='0.29 / W'
+ sa=0 sb=0 sd=0 mult=1 m=1
XM9c VP net41 net42 VDD sky130_fd_pr__pfet_01v8 L=0.5 W=3 nf=1 ad='int((nf+1)/2) * W/nf * 0.29' as='int((nf+2)/2) * W/nf * 0.29'
+ pd='2*int((nf+1)/2) * (W/nf + 0.29)' ps='2*int((nf+2)/2) * (W/nf + 0.29)' nrd='0.29 / W' nrs='0.29 / W'
+ sa=0 sb=0 sd=0 mult=1 m=1
XM9d net42 net41 VP VDD sky130_fd_pr__pfet_01v8 L=0.5 W=3 nf=1 ad='int((nf+1)/2) * W/nf * 0.29' as='int((nf+2)/2) * W/nf * 0.29'
+ pd='2*int((nf+1)/2) * (W/nf + 0.29)' ps='2*int((nf+2)/2) * (W/nf + 0.29)' nrd='0.29 / W' nrs='0.29 / W'
+ sa=0 sb=0 sd=0 mult=1 m=1
XM11a Vcp Vcp net42 VDD sky130_fd_pr__pfet_01v8 L=0.5 W=3 nf=1 ad='int((nf+1)/2) * W/nf * 0.29' as='int((nf+2)/2) * W/nf * 0.29'
+ pd='2*int((nf+1)/2) * (W/nf + 0.29)' ps='2*int((nf+2)/2) * (W/nf + 0.29)' nrd='0.29 / W' nrs='0.29 / W'
+ sa=0 sb=0 sd=0 mult=1 m=1
XM11b net42 Vcp Vcp VDD sky130_fd_pr__pfet_01v8 L=0.5 W=3 nf=1 ad='int((nf+1)/2) * W/nf * 0.29' as='int((nf+2)/2) * W/nf * 0.29'
+ pd='2*int((nf+1)/2) * (W/nf + 0.29)' ps='2*int((nf+2)/2) * (W/nf + 0.29)' nrd='0.29 / W' nrs='0.29 / W'
+ sa=0 sb=0 sd=0 mult=1 m=1
XM11c Vcp Vcp net42 VDD sky130_fd_pr__pfet_01v8 L=0.5 W=3 nf=1 ad='int((nf+1)/2) * W/nf * 0.29' as='int((nf+2)/2) * W/nf * 0.29'
+ pd='2*int((nf+1)/2) * (W/nf + 0.29)' ps='2*int((nf+2)/2) * (W/nf + 0.29)' nrd='0.29 / W' nrs='0.29 / W'
+ sa=0 sb=0 sd=0 mult=1 m=1
XM11d net42 Vcp Vcp VDD sky130_fd_pr__pfet_01v8 L=0.5 W=3 nf=1 ad='int((nf+1)/2) * W/nf * 0.29' as='int((nf+2)/2) * W/nf * 0.29'
+ pd='2*int((nf+1)/2) * (W/nf + 0.29)' ps='2*int((nf+2)/2) * (W/nf + 0.29)' nrd='0.29 / W' nrs='0.29 / W'
+ sa=0 sb=0 sd=0 mult=1 m=1
XM5a Vcn Vcn net40 GND sky130_fd_pr__nfet_01v8 L=0.5 W=3 nf=1 ad='int((nf+1)/2) * W/nf * 0.29' as='int((nf+2)/2) * W/nf * 0.29'
+ pd='2*int((nf+1)/2) * (W/nf + 0.29)' ps='2*int((nf+2)/2) * (W/nf + 0.29)' nrd='0.29 / W' nrs='0.29 / W'
+ sa=0 sb=0 sd=0 mult=1 m=1
XM5b net40 Vcn Vcn GND sky130_fd_pr__nfet_01v8 L=0.5 W=3 nf=1 ad='int((nf+1)/2) * W/nf * 0.29' as='int((nf+2)/2) * W/nf * 0.29'
+ pd='2*int((nf+1)/2) * (W/nf + 0.29)' ps='2*int((nf+2)/2) * (W/nf + 0.29)' nrd='0.29 / W' nrs='0.29 / W'
+ sa=0 sb=0 sd=0 mult=1 m=1
XM5c Vcn Vcn net40 GND sky130_fd_pr__nfet_01v8 L=0.5 W=3 nf=1 ad='int((nf+1)/2) * W/nf * 0.29' as='int((nf+2)/2) * W/nf * 0.29'
+ pd='2*int((nf+1)/2) * (W/nf + 0.29)' ps='2*int((nf+2)/2) * (W/nf + 0.29)' nrd='0.29 / W' nrs='0.29 / W'
+ sa=0 sb=0 sd=0 mult=1 m=1
XM5d net40 Vcn Vcn GND sky130_fd_pr__nfet_01v8 L=0.5 W=3 nf=1 ad='int((nf+1)/2) * W/nf * 0.29' as='int((nf+2)/2) * W/nf * 0.29'
+ pd='2*int((nf+1)/2) * (W/nf + 0.29)' ps='2*int((nf+2)/2) * (W/nf + 0.29)' nrd='0.29 / W' nrs='0.29 / W'
+ sa=0 sb=0 sd=0 mult=1 m=1
XM6a net40 net39 VN GND sky130_fd_pr__nfet_01v8 L=0.5 W=3 nf=1 ad='int((nf+1)/2) * W/nf * 0.29' as='int((nf+2)/2) * W/nf * 0.29'
+ pd='2*int((nf+1)/2) * (W/nf + 0.29)' ps='2*int((nf+2)/2) * (W/nf + 0.29)' nrd='0.29 / W' nrs='0.29 / W'
+ sa=0 sb=0 sd=0 mult=1 m=1
XM6b VN net39 net40 GND sky130_fd_pr__nfet_01v8 L=0.5 W=3 nf=1 ad='int((nf+1)/2) * W/nf * 0.29' as='int((nf+2)/2) * W/nf * 0.29'
+ pd='2*int((nf+1)/2) * (W/nf + 0.29)' ps='2*int((nf+2)/2) * (W/nf + 0.29)' nrd='0.29 / W' nrs='0.29 / W'
+ sa=0 sb=0 sd=0 mult=1 m=1
XM6c net40 net39 VN GND sky130_fd_pr__nfet_01v8 L=0.5 W=3 nf=1 ad='int((nf+1)/2) * W/nf * 0.29' as='int((nf+2)/2) * W/nf * 0.29'
+ pd='2*int((nf+1)/2) * (W/nf + 0.29)' ps='2*int((nf+2)/2) * (W/nf + 0.29)' nrd='0.29 / W' nrs='0.29 / W'
+ sa=0 sb=0 sd=0 mult=1 m=1
XM6d VN net39 net40 GND sky130_fd_pr__nfet_01v8 L=0.5 W=3 nf=1 ad='int((nf+1)/2) * W/nf * 0.29' as='int((nf+2)/2) * W/nf * 0.29'
+ pd='2*int((nf+1)/2) * (W/nf + 0.29)' ps='2*int((nf+2)/2) * (W/nf + 0.29)' nrd='0.29 / W' nrs='0.29 / W'
+ sa=0 sb=0 sd=0 mult=1 m=1
XM8a Vbn Vbn VN GND sky130_fd_pr__nfet_01v8 L=0.5 W=3 nf=1 ad='int((nf+1)/2) * W/nf * 0.29' as='int((nf+2)/2) * W/nf * 0.29'
+ pd='2*int((nf+1)/2) * (W/nf + 0.29)' ps='2*int((nf+2)/2) * (W/nf + 0.29)' nrd='0.29 / W' nrs='0.29 / W'
+ sa=0 sb=0 sd=0 mult=1 m=1
XM8b VN Vbn Vbn GND sky130_fd_pr__nfet_01v8 L=0.5 W=3 nf=1 ad='int((nf+1)/2) * W/nf * 0.29' as='int((nf+2)/2) * W/nf * 0.29'
+ pd='2*int((nf+1)/2) * (W/nf + 0.29)' ps='2*int((nf+2)/2) * (W/nf + 0.29)' nrd='0.29 / W' nrs='0.29 / W'
+ sa=0 sb=0 sd=0 mult=1 m=1
XM8c Vbn Vbn VN GND sky130_fd_pr__nfet_01v8 L=0.5 W=3 nf=1 ad='int((nf+1)/2) * W/nf * 0.29' as='int((nf+2)/2) * W/nf * 0.29'
+ pd='2*int((nf+1)/2) * (W/nf + 0.29)' ps='2*int((nf+2)/2) * (W/nf + 0.29)' nrd='0.29 / W' nrs='0.29 / W'
+ sa=0 sb=0 sd=0 mult=1 m=1
XM8d VN Vbn Vbn GND sky130_fd_pr__nfet_01v8 L=0.5 W=3 nf=1 ad='int((nf+1)/2) * W/nf * 0.29' as='int((nf+2)/2) * W/nf * 0.29'
+ pd='2*int((nf+1)/2) * (W/nf + 0.29)' ps='2*int((nf+2)/2) * (W/nf + 0.29)' nrd='0.29 / W' nrs='0.29 / W'
+ sa=0 sb=0 sd=0 mult=1 m=1
XM13a Vcp Vbn VN GND sky130_fd_pr__nfet_01v8 L=0.5 W=3 nf=1 ad='int((nf+1)/2) * W/nf * 0.29' as='int((nf+2)/2) * W/nf * 0.29'
+ pd='2*int((nf+1)/2) * (W/nf + 0.29)' ps='2*int((nf+2)/2) * (W/nf + 0.29)' nrd='0.29 / W' nrs='0.29 / W'
+ sa=0 sb=0 sd=0 mult=1 m=1
XM13b VN Vbn Vcp GND sky130_fd_pr__nfet_01v8 L=0.5 W=3 nf=1 ad='int((nf+1)/2) * W/nf * 0.29' as='int((nf+2)/2) * W/nf * 0.29'
+ pd='2*int((nf+1)/2) * (W/nf + 0.29)' ps='2*int((nf+2)/2) * (W/nf + 0.29)' nrd='0.29 / W' nrs='0.29 / W'
+ sa=0 sb=0 sd=0 mult=1 m=1
XM13c Vcp Vbn VN GND sky130_fd_pr__nfet_01v8 L=0.5 W=3 nf=1 ad='int((nf+1)/2) * W/nf * 0.29' as='int((nf+2)/2) * W/nf * 0.29'
+ pd='2*int((nf+1)/2) * (W/nf + 0.29)' ps='2*int((nf+2)/2) * (W/nf + 0.29)' nrd='0.29 / W' nrs='0.29 / W'
+ sa=0 sb=0 sd=0 mult=1 m=1
XM13d VN Vbn Vcp GND sky130_fd_pr__nfet_01v8 L=0.5 W=3 nf=1 ad='int((nf+1)/2) * W/nf * 0.29' as='int((nf+2)/2) * W/nf * 0.29'
+ pd='2*int((nf+1)/2) * (W/nf + 0.29)' ps='2*int((nf+2)/2) * (W/nf + 0.29)' nrd='0.29 / W' nrs='0.29 / W'
+ sa=0 sb=0 sd=0 mult=1 m=1
XM2 VP VP net39 VDD sky130_fd_pr__pfet_01v8 L=0.5 W=3 nf=1 ad='int((nf+1)/2) * W/nf * 0.29' as='int((nf+2)/2) * W/nf * 0.29'
+ pd='2*int((nf+1)/2) * (W/nf + 0.29)' ps='2*int((nf+2)/2) * (W/nf + 0.29)' nrd='0.29 / W' nrs='0.29 / W'
+ sa=0 sb=0 sd=0 mult=1 m=1
XM3 VP VP VP VDD sky130_fd_pr__pfet_01v8 L=0.5 W=3 nf=1 ad='int((nf+1)/2) * W/nf * 0.29' as='int((nf+2)/2) * W/nf * 0.29'
+ pd='2*int((nf+1)/2) * (W/nf + 0.29)' ps='2*int((nf+2)/2) * (W/nf + 0.29)' nrd='0.29 / W' nrs='0.29 / W'
+ sa=0 sb=0 sd=0 mult=1 m=1
XM4 VP VP VP VDD sky130_fd_pr__pfet_01v8 L=0.5 W=3 nf=1 ad='int((nf+1)/2) * W/nf * 0.29' as='int((nf+2)/2) * W/nf * 0.29'
+ pd='2*int((nf+1)/2) * (W/nf + 0.29)' ps='2*int((nf+2)/2) * (W/nf + 0.29)' nrd='0.29 / W' nrs='0.29 / W'
+ sa=0 sb=0 sd=0 mult=1 m=1
XM5 VN VN VN GND sky130_fd_pr__nfet_01v8 L=0.5 W=3 nf=1 ad='int((nf+1)/2) * W/nf * 0.29' as='int((nf+2)/2) * W/nf * 0.29'
+ pd='2*int((nf+1)/2) * (W/nf + 0.29)' ps='2*int((nf+2)/2) * (W/nf + 0.29)' nrd='0.29 / W' nrs='0.29 / W'
+ sa=0 sb=0 sd=0 mult=1 m=1
XM6 net40 VN VN GND sky130_fd_pr__nfet_01v8 L=0.5 W=3 nf=1 ad='int((nf+1)/2) * W/nf * 0.29' as='int((nf+2)/2) * W/nf * 0.29'
+ pd='2*int((nf+1)/2) * (W/nf + 0.29)' ps='2*int((nf+2)/2) * (W/nf + 0.29)' nrd='0.29 / W' nrs='0.29 / W'
+ sa=0 sb=0 sd=0 mult=1 m=1
XM8 VN VN VN GND sky130_fd_pr__nfet_01v8 L=0.5 W=3 nf=1 ad='int((nf+1)/2) * W/nf * 0.29' as='int((nf+2)/2) * W/nf * 0.29'
+ pd='2*int((nf+1)/2) * (W/nf + 0.29)' ps='2*int((nf+2)/2) * (W/nf + 0.29)' nrd='0.29 / W' nrs='0.29 / W'
+ sa=0 sb=0 sd=0 mult=1 m=1
XM9 VN VN net40 GND sky130_fd_pr__nfet_01v8 L=0.5 W=3 nf=1 ad='int((nf+1)/2) * W/nf * 0.29' as='int((nf+2)/2) * W/nf * 0.29'
+ pd='2*int((nf+1)/2) * (W/nf + 0.29)' ps='2*int((nf+2)/2) * (W/nf + 0.29)' nrd='0.29 / W' nrs='0.29 / W'
+ sa=0 sb=0 sd=0 mult=1 m=1
XM10 VP VP VP VDD sky130_fd_pr__pfet_01v8 L=0.5 W=3 nf=1 ad='int((nf+1)/2) * W/nf * 0.29' as='int((nf+2)/2) * W/nf * 0.29'
+ pd='2*int((nf+1)/2) * (W/nf + 0.29)' ps='2*int((nf+2)/2) * (W/nf + 0.29)' nrd='0.29 / W' nrs='0.29 / W'
+ sa=0 sb=0 sd=0 mult=1 m=1
XM11 VP VP Vcp VDD sky130_fd_pr__pfet_01v8 L=0.5 W=3 nf=1 ad='int((nf+1)/2) * W/nf * 0.29' as='int((nf+2)/2) * W/nf * 0.29'
+ pd='2*int((nf+1)/2) * (W/nf + 0.29)' ps='2*int((nf+2)/2) * (W/nf + 0.29)' nrd='0.29 / W' nrs='0.29 / W'
+ sa=0 sb=0 sd=0 mult=1 m=1
XM12 VN VN VN GND sky130_fd_pr__nfet_01v8 L=0.5 W=3 nf=1 ad='int((nf+1)/2) * W/nf * 0.29' as='int((nf+2)/2) * W/nf * 0.29'
+ pd='2*int((nf+1)/2) * (W/nf + 0.29)' ps='2*int((nf+2)/2) * (W/nf + 0.29)' nrd='0.29 / W' nrs='0.29 / W'
+ sa=0 sb=0 sd=0 mult=1 m=1
XM13 VN VN VN GND sky130_fd_pr__nfet_01v8 L=0.5 W=3 nf=1 ad='int((nf+1)/2) * W/nf * 0.29' as='int((nf+2)/2) * W/nf * 0.29'
+ pd='2*int((nf+1)/2) * (W/nf + 0.29)' ps='2*int((nf+2)/2) * (W/nf + 0.29)' nrd='0.29 / W' nrs='0.29 / W'
+ sa=0 sb=0 sd=0 mult=1 m=1
XM14 net41 VN VN GND sky130_fd_pr__nfet_01v8 L=0.5 W=3 nf=1 ad='int((nf+1)/2) * W/nf * 0.29' as='int((nf+2)/2) * W/nf * 0.29'
+ pd='2*int((nf+1)/2) * (W/nf + 0.29)' ps='2*int((nf+2)/2) * (W/nf + 0.29)' nrd='0.29 / W' nrs='0.29 / W'
+ sa=0 sb=0 sd=0 mult=1 m=1
XM15 VN VN VN GND sky130_fd_pr__nfet_01v8 L=0.5 W=3 nf=1 ad='int((nf+1)/2) * W/nf * 0.29' as='int((nf+2)/2) * W/nf * 0.29'
+ pd='2*int((nf+1)/2) * (W/nf + 0.29)' ps='2*int((nf+2)/2) * (W/nf + 0.29)' nrd='0.29 / W' nrs='0.29 / W'
+ sa=0 sb=0 sd=0 mult=1 m=1
XM1 Vbp Vbp VP VDD sky130_fd_pr__pfet_01v8 L=0.5 W=3 nf=1 ad='int((nf+1)/2) * W/nf * 0.29' as='int((nf+2)/2) * W/nf * 0.29'
+ pd='2*int((nf+1)/2) * (W/nf + 0.29)' ps='2*int((nf+2)/2) * (W/nf + 0.29)' nrd='0.29 / W' nrs='0.29 / W'
+ sa=0 sb=0 sd=0 mult=1 m=1
XM7 VP Vbp Vbp VDD sky130_fd_pr__pfet_01v8 L=0.5 W=3 nf=1 ad='int((nf+1)/2) * W/nf * 0.29' as='int((nf+2)/2) * W/nf * 0.29'
+ pd='2*int((nf+1)/2) * (W/nf + 0.29)' ps='2*int((nf+2)/2) * (W/nf + 0.29)' nrd='0.29 / W' nrs='0.29 / W'
+ sa=0 sb=0 sd=0 mult=1 m=1
XM16 Vbp Vbp VP VDD sky130_fd_pr__pfet_01v8 L=0.5 W=3 nf=1 ad='int((nf+1)/2) * W/nf * 0.29' as='int((nf+2)/2) * W/nf * 0.29'
+ pd='2*int((nf+1)/2) * (W/nf + 0.29)' ps='2*int((nf+2)/2) * (W/nf + 0.29)' nrd='0.29 / W' nrs='0.29 / W'
+ sa=0 sb=0 sd=0 mult=1 m=1
XM17 VP Vbp net43 VDD sky130_fd_pr__pfet_01v8 L=0.5 W=3 nf=1 ad='int((nf+1)/2) * W/nf * 0.29' as='int((nf+2)/2) * W/nf * 0.29'
+ pd='2*int((nf+1)/2) * (W/nf + 0.29)' ps='2*int((nf+2)/2) * (W/nf + 0.29)' nrd='0.29 / W' nrs='0.29 / W'
+ sa=0 sb=0 sd=0 mult=1 m=1
XM18 net43 VP VP VDD sky130_fd_pr__pfet_01v8 L=0.5 W=3 nf=1 ad='int((nf+1)/2) * W/nf * 0.29' as='int((nf+2)/2) * W/nf * 0.29'
+ pd='2*int((nf+1)/2) * (W/nf + 0.29)' ps='2*int((nf+2)/2) * (W/nf + 0.29)' nrd='0.29 / W' nrs='0.29 / W'
+ sa=0 sb=0 sd=0 mult=1 m=1
XM19 VP VP Vbp VDD sky130_fd_pr__pfet_01v8 L=0.5 W=3 nf=1 ad='int((nf+1)/2) * W/nf * 0.29' as='int((nf+2)/2) * W/nf * 0.29'
+ pd='2*int((nf+1)/2) * (W/nf + 0.29)' ps='2*int((nf+2)/2) * (W/nf + 0.29)' nrd='0.29 / W' nrs='0.29 / W'
+ sa=0 sb=0 sd=0 mult=1 m=1
XM20 VN VN VN GND sky130_fd_pr__nfet_01v8 L=0.5 W=3 nf=1 ad='int((nf+1)/2) * W/nf * 0.29' as='int((nf+2)/2) * W/nf * 0.29'
+ pd='2*int((nf+1)/2) * (W/nf + 0.29)' ps='2*int((nf+2)/2) * (W/nf + 0.29)' nrd='0.29 / W' nrs='0.29 / W'
+ sa=0 sb=0 sd=0 mult=1 m=1
XM21 VP VP VP VDD sky130_fd_pr__pfet_01v8 L=0.5 W=3 nf=1 ad='int((nf+1)/2) * W/nf * 0.29' as='int((nf+2)/2) * W/nf * 0.29'
+ pd='2*int((nf+1)/2) * (W/nf + 0.29)' ps='2*int((nf+2)/2) * (W/nf + 0.29)' nrd='0.29 / W' nrs='0.29 / W'
+ sa=0 sb=0 sd=0 mult=1 m=1
XM22 VN VN VN GND sky130_fd_pr__nfet_01v8 L=0.5 W=3 nf=1 ad='int((nf+1)/2) * W/nf * 0.29' as='int((nf+2)/2) * W/nf * 0.29'
+ pd='2*int((nf+1)/2) * (W/nf + 0.29)' ps='2*int((nf+2)/2) * (W/nf + 0.29)' nrd='0.29 / W' nrs='0.29 / W'
+ sa=0 sb=0 sd=0 mult=1 m=1
XM23 VP VP VP VDD sky130_fd_pr__pfet_01v8 L=0.5 W=3 nf=1 ad='int((nf+1)/2) * W/nf * 0.29' as='int((nf+2)/2) * W/nf * 0.29'
+ pd='2*int((nf+1)/2) * (W/nf + 0.29)' ps='2*int((nf+2)/2) * (W/nf + 0.29)' nrd='0.29 / W' nrs='0.29 / W'
+ sa=0 sb=0 sd=0 mult=1 m=1
XM24 VP VP VP VDD sky130_fd_pr__pfet_01v8 L=0.5 W=3 nf=1 ad='int((nf+1)/2) * W/nf * 0.29' as='int((nf+2)/2) * W/nf * 0.29'
+ pd='2*int((nf+1)/2) * (W/nf + 0.29)' ps='2*int((nf+2)/2) * (W/nf + 0.29)' nrd='0.29 / W' nrs='0.29 / W'
+ sa=0 sb=0 sd=0 mult=1 m=1
XM25 VP VP VP VDD sky130_fd_pr__pfet_01v8 L=0.5 W=3 nf=1 ad='int((nf+1)/2) * W/nf * 0.29' as='int((nf+2)/2) * W/nf * 0.29'
+ pd='2*int((nf+1)/2) * (W/nf + 0.29)' ps='2*int((nf+2)/2) * (W/nf + 0.29)' nrd='0.29 / W' nrs='0.29 / W'
+ sa=0 sb=0 sd=0 mult=1 m=1
XM26 Vcp VP VP VDD sky130_fd_pr__pfet_01v8 L=0.5 W=3 nf=1 ad='int((nf+1)/2) * W/nf * 0.29' as='int((nf+2)/2) * W/nf * 0.29'
+ pd='2*int((nf+1)/2) * (W/nf + 0.29)' ps='2*int((nf+2)/2) * (W/nf + 0.29)' nrd='0.29 / W' nrs='0.29 / W'
+ sa=0 sb=0 sd=0 mult=1 m=1
**.ends
.end
